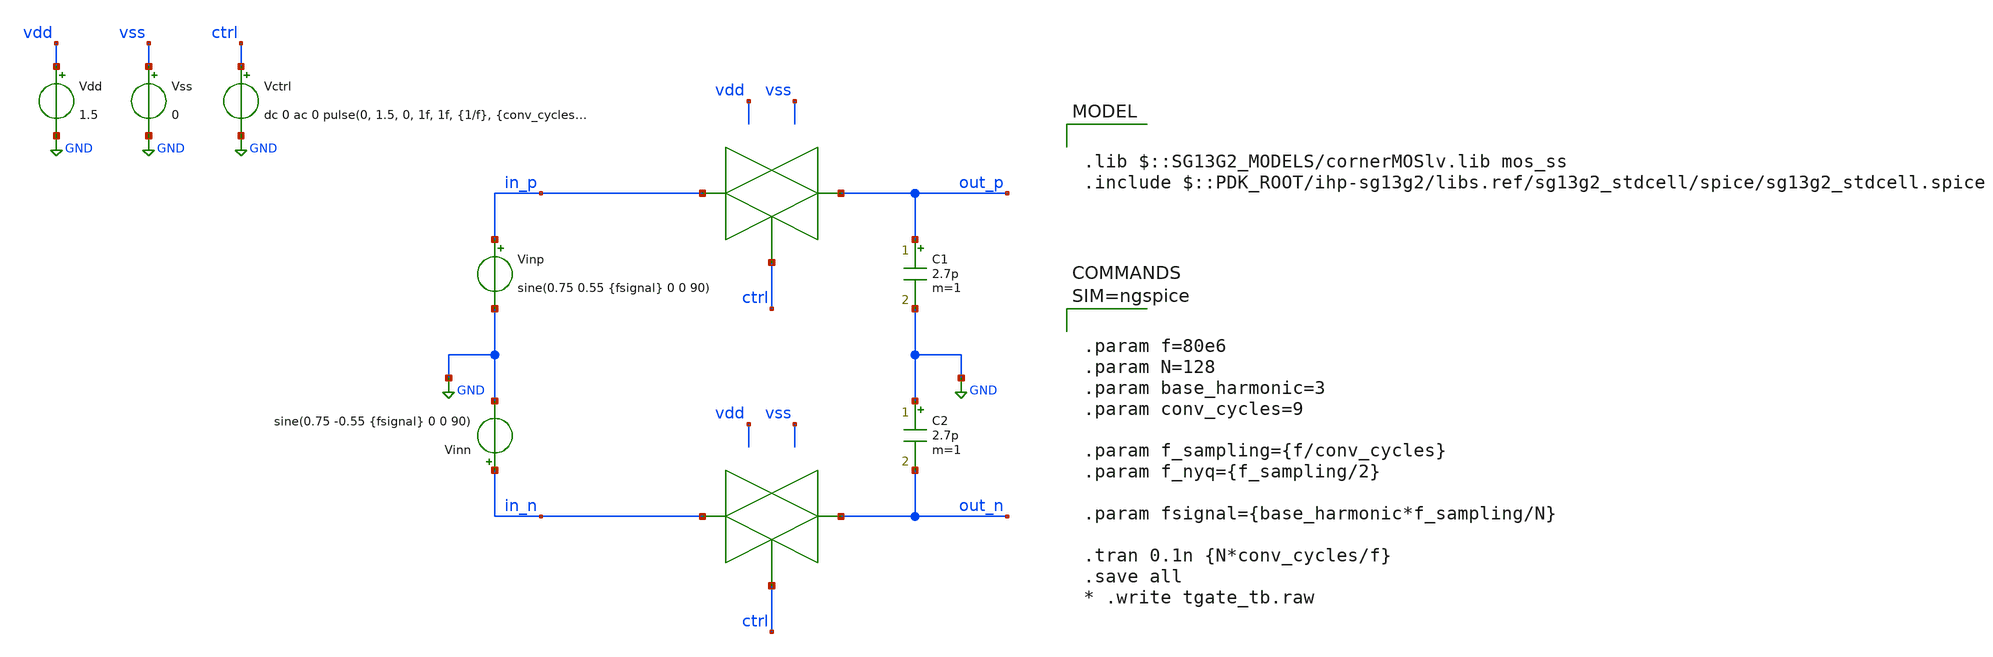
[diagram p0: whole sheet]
** sch_path: designs/tgate_slow/tgate_tb.sch
**.subckt tgate_tb
Vdd vdd GND 1.5
Vss vss GND 0
C1 out_p GND 2.7p m=1
Vinp in_p GND sine(0.75 0.55 {fsignal} 0 0 90)
C2 GND out_n 2.7p m=1
Vinn in_n GND sine(0.75 -0.55 {fsignal} 0 0 90)
Vctrl ctrl GND dc 0 ac 0 pulse(0, 1.5, 0, 1f, 1f, {1/f}, {conv_cycles/f})
**** begin user architecture code



.param f=80e6
.param N=128
.param base_harmonic=3
.param conv_cycles=9

.param f_sampling={f/conv_cycles}
.param f_nyq={f_sampling/2}

.param fsignal={base_harmonic*f_sampling/N}

.tran 0.1n {N*conv_cycles/f}
.save all
* .write tgate_tb.raw




.lib $::SG13G2_MODELS/cornerMOSlv.lib mos_ss
.include $::PDK_ROOT/ihp-sg13g2/libs.ref/sg13g2_stdcell/spice/sg13g2_stdcell.spice

**** end user architecture code
**.ends
.GLOBAL GND
.end
